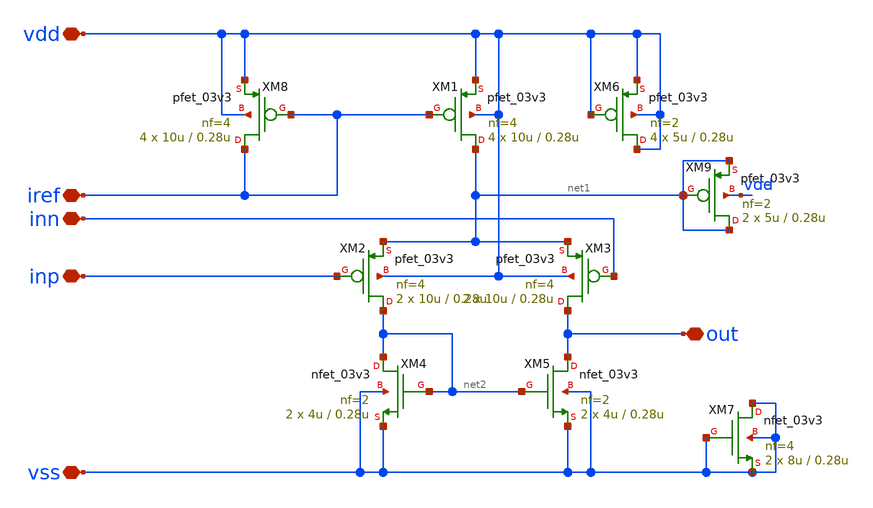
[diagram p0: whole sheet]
** sch_path: designs/libs/qw_core_analog/OTAforChargePump/OTAforChargePump.sch
**.subckt OTAforChargePump inp inn vdd vss out iref
*.iopin inp
*.iopin inn
*.iopin vdd
*.iopin vss
*.iopin out
*.iopin iref
XM8 iref iref vdd vdd pfet_03v3 L=0.28u W=10u nf=4 ad='int((nf+1)/2) * W/nf * 0.18u' as='int((nf+2)/2) * W/nf * 0.18u'
+ pd='2*int((nf+1)/2) * (W/nf + 0.18u)' ps='2*int((nf+2)/2) * (W/nf + 0.18u)' nrd='0.18u / W' nrs='0.18u / W'
+ sa=0 sb=0 sd=0 m=4
XM1 net1 iref vdd vdd pfet_03v3 L=0.28u W=10u nf=4 ad='int((nf+1)/2) * W/nf * 0.18u' as='int((nf+2)/2) * W/nf * 0.18u'
+ pd='2*int((nf+1)/2) * (W/nf + 0.18u)' ps='2*int((nf+2)/2) * (W/nf + 0.18u)' nrd='0.18u / W' nrs='0.18u / W'
+ sa=0 sb=0 sd=0 m=4
XM2 net2 inp net1 vdd pfet_03v3 L=0.28u W=10u nf=4 ad='int((nf+1)/2) * W/nf * 0.18u' as='int((nf+2)/2) * W/nf * 0.18u'
+ pd='2*int((nf+1)/2) * (W/nf + 0.18u)' ps='2*int((nf+2)/2) * (W/nf + 0.18u)' nrd='0.18u / W' nrs='0.18u / W'
+ sa=0 sb=0 sd=0 m=2
XM3 out inn net1 vdd pfet_03v3 L=0.28u W=10u nf=4 ad='int((nf+1)/2) * W/nf * 0.18u' as='int((nf+2)/2) * W/nf * 0.18u'
+ pd='2*int((nf+1)/2) * (W/nf + 0.18u)' ps='2*int((nf+2)/2) * (W/nf + 0.18u)' nrd='0.18u / W' nrs='0.18u / W'
+ sa=0 sb=0 sd=0 m=2
XM4 net2 net2 vss vss nfet_03v3 L=0.28u W=4u nf=2 ad='int((nf+1)/2) * W/nf * 0.18u' as='int((nf+2)/2) * W/nf * 0.18u'
+ pd='2*int((nf+1)/2) * (W/nf + 0.18u)' ps='2*int((nf+2)/2) * (W/nf + 0.18u)' nrd='0.18u / W' nrs='0.18u / W'
+ sa=0 sb=0 sd=0 m=2
XM5 out net2 vss vss nfet_03v3 L=0.28u W=4u nf=2 ad='int((nf+1)/2) * W/nf * 0.18u' as='int((nf+2)/2) * W/nf * 0.18u'
+ pd='2*int((nf+1)/2) * (W/nf + 0.18u)' ps='2*int((nf+2)/2) * (W/nf + 0.18u)' nrd='0.18u / W' nrs='0.18u / W'
+ sa=0 sb=0 sd=0 m=2
XM6 vdd vdd vdd vdd pfet_03v3 L=0.28u W=5u nf=2 ad='int((nf+1)/2) * W/nf * 0.18u' as='int((nf+2)/2) * W/nf * 0.18u'
+ pd='2*int((nf+1)/2) * (W/nf + 0.18u)' ps='2*int((nf+2)/2) * (W/nf + 0.18u)' nrd='0.18u / W' nrs='0.18u / W'
+ sa=0 sb=0 sd=0 m=4
XM7 vss vss vss vss nfet_03v3 L=0.28u W=8u nf=4 ad='int((nf+1)/2) * W/nf * 0.18u' as='int((nf+2)/2) * W/nf * 0.18u'
+ pd='2*int((nf+1)/2) * (W/nf + 0.18u)' ps='2*int((nf+2)/2) * (W/nf + 0.18u)' nrd='0.18u / W' nrs='0.18u / W'
+ sa=0 sb=0 sd=0 m=2
XM9 net1 net1 net1 vdd pfet_03v3 L=0.28u W=5u nf=2 ad='int((nf+1)/2) * W/nf * 0.18u' as='int((nf+2)/2) * W/nf * 0.18u'
+ pd='2*int((nf+1)/2) * (W/nf + 0.18u)' ps='2*int((nf+2)/2) * (W/nf + 0.18u)' nrd='0.18u / W' nrs='0.18u / W'
+ sa=0 sb=0 sd=0 m=2
**.ends
.end
